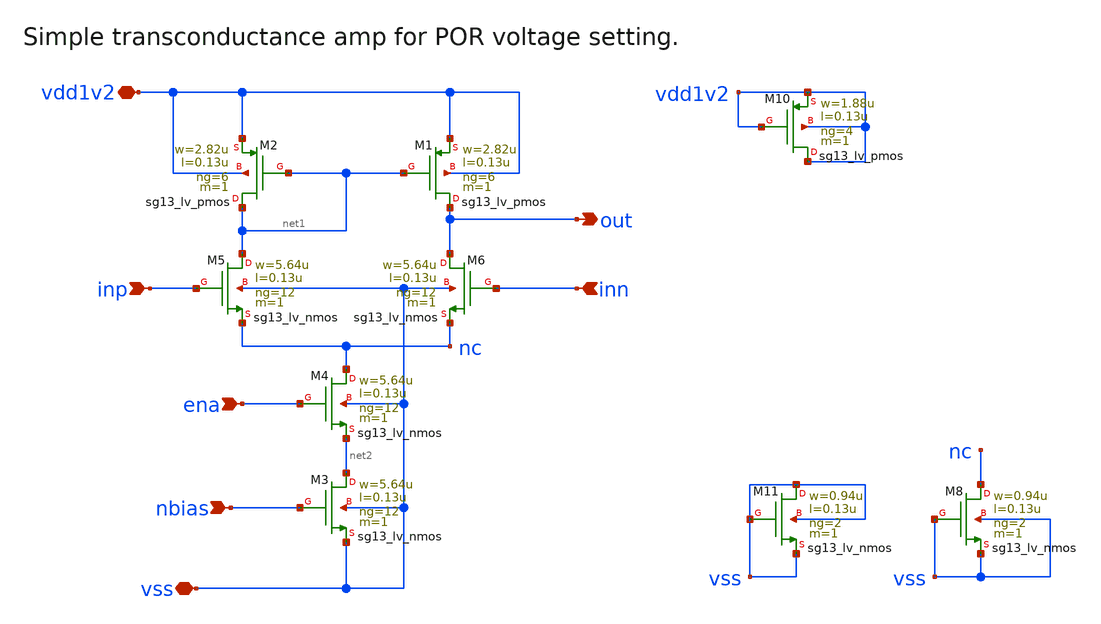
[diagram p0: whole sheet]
** sch_path: xschem/por_amp.sch
**.subckt por_amp ena inp inn out vdd1v2 vss nbias
*.ipin ena
*.ipin inp
*.ipin inn
*.opin out
*.iopin vdd1v2
*.iopin vss
*.ipin nbias
XM10 vdd1v2 vdd1v2 vdd1v2 vdd1v2 sg13_lv_pmos w=1.88u l=0.13u ng=4 m=1 mm_ok=1
XM11 vss vss vss vss sg13_lv_nmos w=0.94u l=0.13u ng=2 m=1 mm_ok=1
XM8 nc vss vss vss sg13_lv_nmos w=0.94u l=0.13u ng=2 m=1 mm_ok=1
XM1 out net1 vdd1v2 vdd1v2 sg13_lv_pmos w=2.82u l=0.13u ng=6 m=1 mm_ok=1
XM2 net1 net1 vdd1v2 vdd1v2 sg13_lv_pmos w=2.82u l=0.13u ng=6 m=1 mm_ok=1
XM3 net2 nbias vss vss sg13_lv_nmos w=5.64u l=0.13u ng=12 m=1 mm_ok=1
XM4 nc ena net2 vss sg13_lv_nmos w=5.64u l=0.13u ng=12 m=1 mm_ok=1
XM5 net1 inp nc vss sg13_lv_nmos w=5.64u l=0.13u ng=12 m=1 mm_ok=1
XM6 out inn nc vss sg13_lv_nmos w=5.64u l=0.13u ng=12 m=1 mm_ok=1
**.ends
.end
